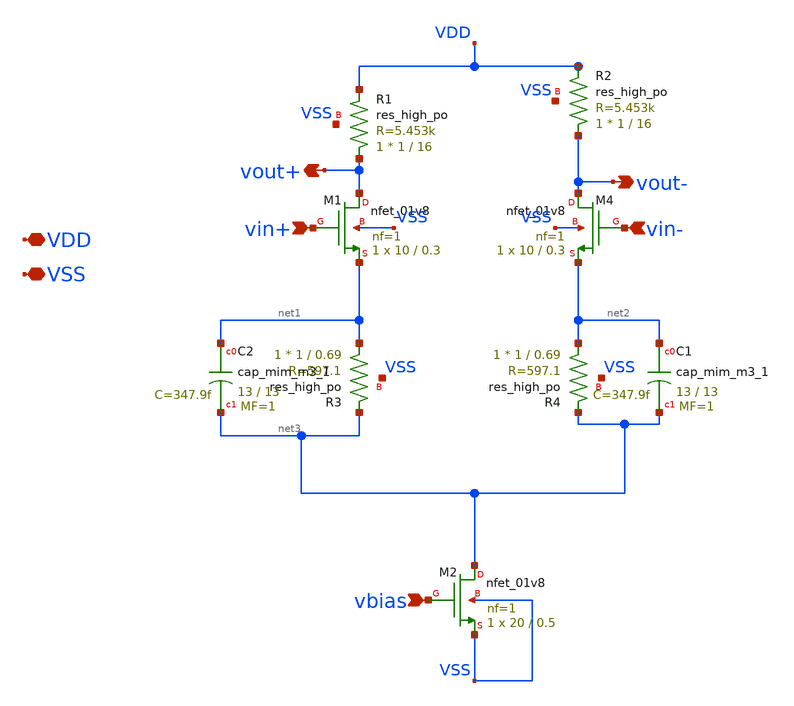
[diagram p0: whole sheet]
** sch_path: xschem/CTLE.sch
**.subckt CTLE VDD VSS vin+ vin- vbias vout- vout+
*.iopin VDD
*.iopin VSS
*.ipin vin+
*.ipin vin-
*.ipin vbias
*.opin vout-
*.opin vout+
XM1 vout+ vin+ net1 VSS sky130_fd_pr__nfet_01v8 L=0.3 W=10 nf=1 ad='int((nf+1)/2) * W/nf * 0.29' as='int((nf+2)/2) * W/nf * 0.29'
+ pd='2*int((nf+1)/2) * (W/nf + 0.29)' ps='2*int((nf+2)/2) * (W/nf + 0.29)' nrd='0.29 / W' nrs='0.29 / W'
+ sa=0 sb=0 sd=0 mult=1 m=1
XM2 net3 vbias VSS VSS sky130_fd_pr__nfet_01v8 L=0.5 W=20 nf=1 ad='int((nf+1)/2) * W/nf * 0.29' as='int((nf+2)/2) * W/nf * 0.29'
+ pd='2*int((nf+1)/2) * (W/nf + 0.29)' ps='2*int((nf+2)/2) * (W/nf + 0.29)' nrd='0.29 / W' nrs='0.29 / W'
+ sa=0 sb=0 sd=0 mult=1 m=1
XM4 vout- vin- net2 VSS sky130_fd_pr__nfet_01v8 L=0.3 W=10 nf=1 ad='int((nf+1)/2) * W/nf * 0.29' as='int((nf+2)/2) * W/nf * 0.29'
+ pd='2*int((nf+1)/2) * (W/nf + 0.29)' ps='2*int((nf+2)/2) * (W/nf + 0.29)' nrd='0.29 / W' nrs='0.29 / W'
+ sa=0 sb=0 sd=0 mult=1 m=1
XR1 vout+ VDD VSS sky130_fd_pr__res_high_po W=1 L=16 mult=1 m=1
XR2 vout- VDD VSS sky130_fd_pr__res_high_po W=1 L=16 mult=1 m=1
XR3 net1 net3 VSS sky130_fd_pr__res_high_po W=1 L=0.69 mult=1 m=1
XC2 net1 net3 sky130_fd_pr__cap_mim_m3_1 W=13 L=13 MF=1 m=1
XR4 net2 net3 VSS sky130_fd_pr__res_high_po W=1 L=0.69 mult=1 m=1
XC1 net2 net3 sky130_fd_pr__cap_mim_m3_1 W=13 L=13 MF=1 m=1
**.ends
.end
